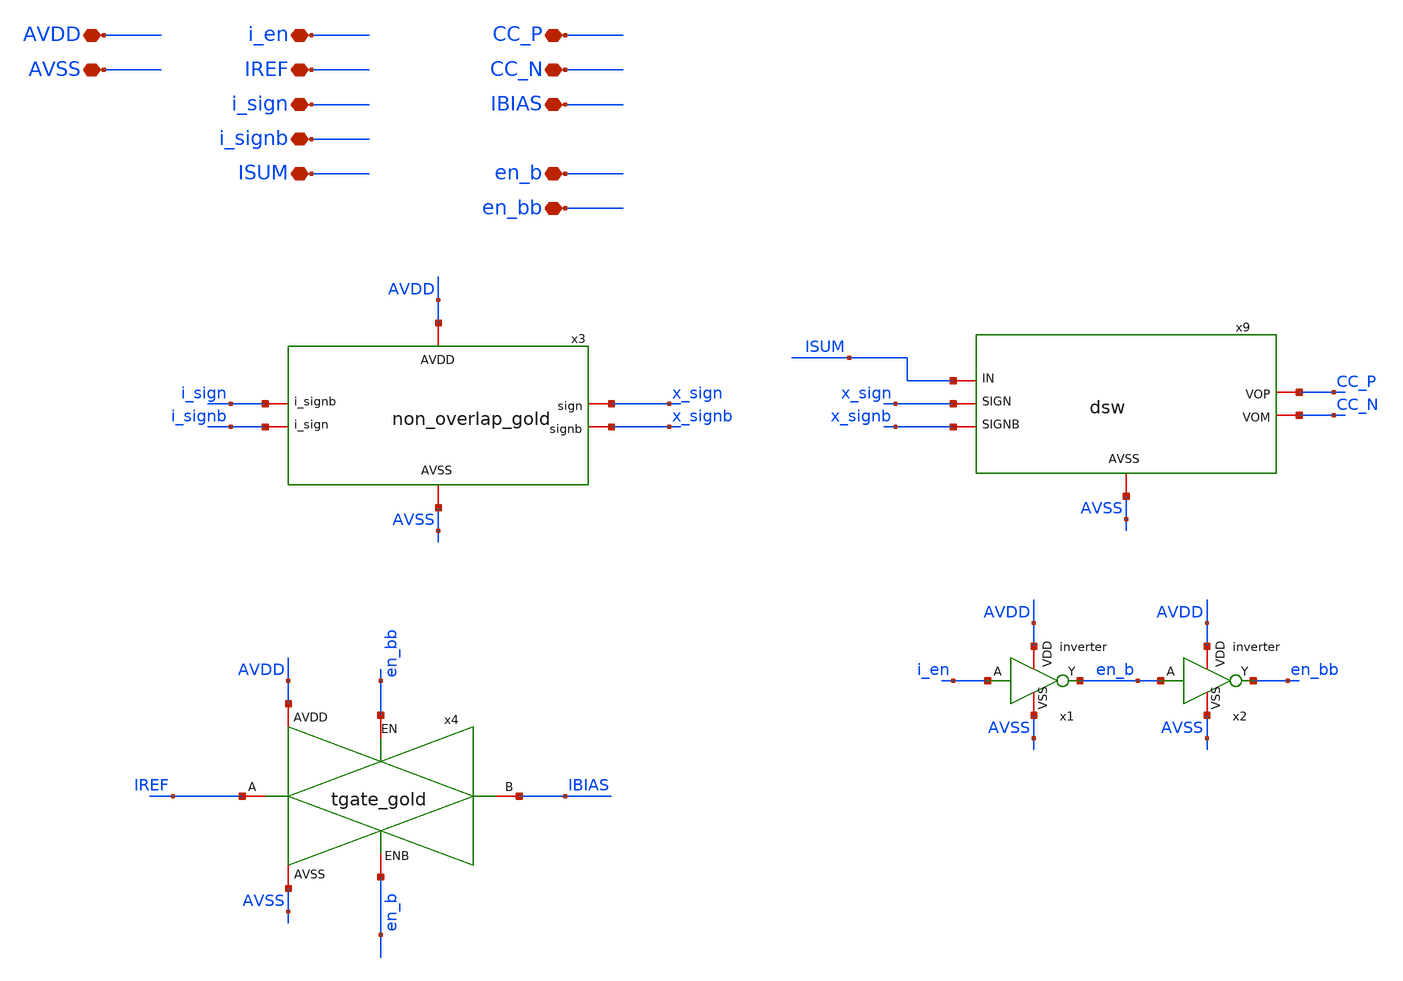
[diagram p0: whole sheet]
** sch_path: current_generator/analog/DAC/schematics/sub_top_gold_orig.sch
**.subckt sub_top_gold_orig AVDD AVSS i_en i_sign i_signb ISUM CC_P CC_N IREF IBIAS en_b en_bb
*.iopin AVDD
*.iopin AVSS
*.iopin i_en
*.iopin i_sign
*.iopin i_signb
*.iopin ISUM
*.iopin CC_P
*.iopin CC_N
*.iopin IREF
*.iopin IBIAS
*.iopin en_b
*.iopin en_bb
x9 x_sign x_signb ISUM AVSS CC_P CC_N dsw
x1 i_en en_b AVDD AVSS inverter
x2 en_b en_bb AVDD AVSS inverter
x4 AVDD AVSS en_bb en_b IREF IBIAS tgate_gold
x3 AVDD AVSS i_signb i_sign x_sign x_signb non_overlap_gold
**.ends
.end
